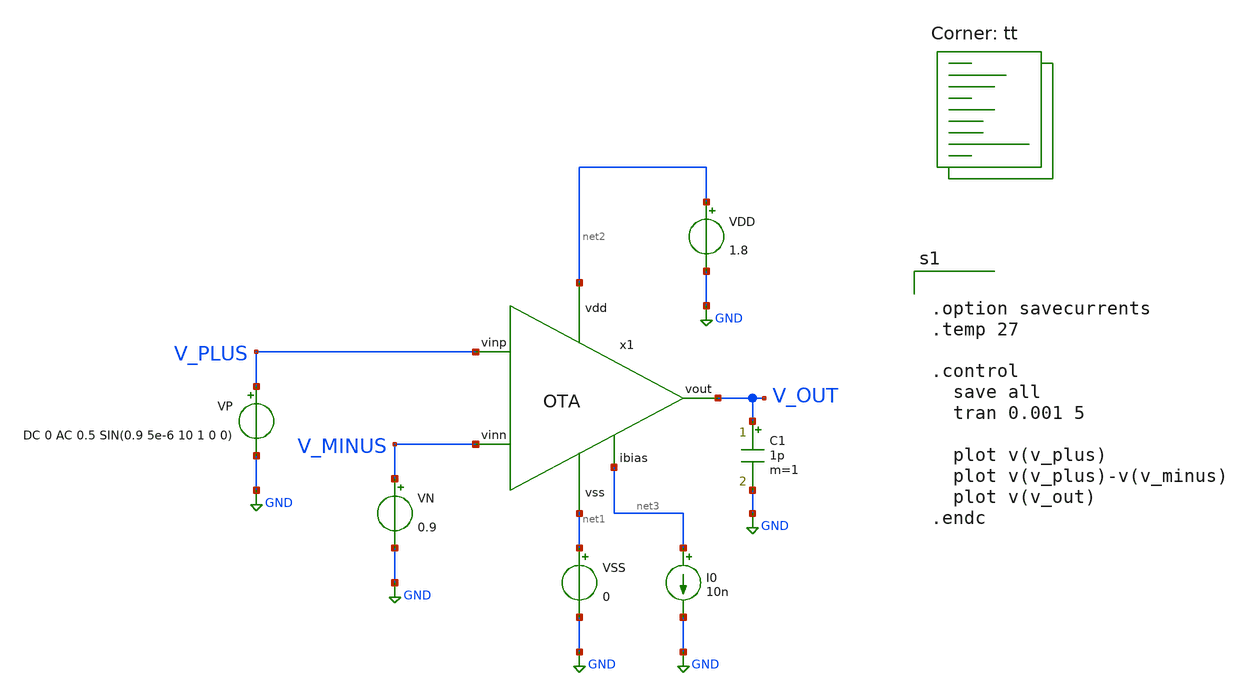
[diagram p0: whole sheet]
** sch_path: Schematic/OTA_Trans_tb.sch
**.subckt OTA_Trans_tb
x1 net2 V_OUT net3 V_MINUS V_PLUS net1 OTA
VDD net2 GND 1.8
VP V_PLUS GND DC 0 AC 0.5 SIN(0.9 5e-6 10 1 0 0)
VN V_MINUS GND 0.9
VSS net1 GND 0
I0 net3 GND 10n
C1 V_OUT GND 1p m=1
**** begin user architecture code


.option savecurrents
.temp 27

.control
  save all
  tran 0.001 5

  plot v(v_plus)
  plot v(v_plus)-v(v_minus)
  plot v(v_out)
.endc



.lib $::SKYWATER_MODELS/sky130.lib.spice tt
**** end user architecture code
**.ends

* expanding   symbol:  /foss/designs/Neuromorphics/Analog_to_Spike/Schematic/OTA.sym # of pins=6
** sym_path: Schematic/OTA.sym
** sch_path: Schematic/OTA.sch
.subckt OTA vdd vout ibias vinn vinp vss
*.ipin vdd
*.ipin vinp
*.ipin vinn
*.ipin vss
*.opin vout
*.ipin ibias
XM1 net1 vinp net3 vdd sky130_fd_pr__pfet_01v8 L=2 W=10 nf=1 ad='int((1 + 1)/2) * 10 / 1 * 0.29' as='int((1 + 2)/2) * 10 / 1 * 0.29'
+ pd='2*int((1 + 1)/2) * (10 / 1 + 0.29)' ps='2*int((1 + 2)/2) * (10 / 1 + 0.29)' nrd='0.29 / 10 ' nrs='0.29 / 10 '
+ sa=0 sb=0 sd=0 mult=1 m=1
XM3 net1 net1 vss vss sky130_fd_pr__nfet_01v8 L=2 W=2 nf=1 ad='int((1 + 1)/2) * 2 / 1 * 0.29' as='int((1 + 2)/2) * 2 / 1 * 0.29'
+ pd='2*int((1 + 1)/2) * (2 / 1 + 0.29)' ps='2*int((1 + 2)/2) * (2 / 1 + 0.29)' nrd='0.29 / 2 ' nrs='0.29 / 2 '
+ sa=0 sb=0 sd=0 mult=1 m=1
XM4 net2 net2 vss vss sky130_fd_pr__nfet_01v8 L=2 W=2 nf=1 ad='int((1 + 1)/2) * 2 / 1 * 0.29' as='int((1 + 2)/2) * 2 / 1 * 0.29'
+ pd='2*int((1 + 1)/2) * (2 / 1 + 0.29)' ps='2*int((1 + 2)/2) * (2 / 1 + 0.29)' nrd='0.29 / 2 ' nrs='0.29 / 2 '
+ sa=0 sb=0 sd=0 mult=1 m=1
XM2 net2 vinn net3 vdd sky130_fd_pr__pfet_01v8 L=2 W=10 nf=1 ad='int((1 + 1)/2) * 10 / 1 * 0.29' as='int((1 + 2)/2) * 10 / 1 * 0.29'
+ pd='2*int((1 + 1)/2) * (10 / 1 + 0.29)' ps='2*int((1 + 2)/2) * (10 / 1 + 0.29)' nrd='0.29 / 10 ' nrs='0.29 / 10 '
+ sa=0 sb=0 sd=0 mult=1 m=1
XM5 net4 net1 vss vss sky130_fd_pr__nfet_01v8 L=2 W=14 nf=1 ad='int((1 + 1)/2) * 14 / 1 * 0.29' as='int((1 + 2)/2) * 14 / 1 * 0.29'
+ pd='2*int((1 + 1)/2) * (14 / 1 + 0.29)' ps='2*int((1 + 2)/2) * (14 / 1 + 0.29)' nrd='0.29 / 14 ' nrs='0.29 / 14 '
+ sa=0 sb=0 sd=0 mult=1 m=1
XM6 vout net2 vss vss sky130_fd_pr__nfet_01v8 L=2 W=14 nf=1 ad='int((1 + 1)/2) * 14 / 1 * 0.29' as='int((1 + 2)/2) * 14 / 1 * 0.29'
+ pd='2*int((1 + 1)/2) * (14 / 1 + 0.29)' ps='2*int((1 + 2)/2) * (14 / 1 + 0.29)' nrd='0.29 / 14 ' nrs='0.29 / 14 '
+ sa=0 sb=0 sd=0 mult=1 m=1
XM7 net4 net4 vdd vdd sky130_fd_pr__pfet_01v8 L=2 W=2 nf=1 ad='int((1 + 1)/2) * 2 / 1 * 0.29' as='int((1 + 2)/2) * 2 / 1 * 0.29'
+ pd='2*int((1 + 1)/2) * (2 / 1 + 0.29)' ps='2*int((1 + 2)/2) * (2 / 1 + 0.29)' nrd='0.29 / 2 ' nrs='0.29 / 2 '
+ sa=0 sb=0 sd=0 mult=1 m=1
XM8 vout net4 vdd vdd sky130_fd_pr__pfet_01v8 L=2 W=2 nf=1 ad='int((1 + 1)/2) * 2 / 1 * 0.29' as='int((1 + 2)/2) * 2 / 1 * 0.29'
+ pd='2*int((1 + 1)/2) * (2 / 1 + 0.29)' ps='2*int((1 + 2)/2) * (2 / 1 + 0.29)' nrd='0.29 / 2 ' nrs='0.29 / 2 '
+ sa=0 sb=0 sd=0 mult=1 m=1
XM10 net3 ibias vdd vdd sky130_fd_pr__pfet_01v8 L=2 W=10 nf=1 ad='int((1 + 1)/2) * 10 / 1 * 0.29' as='int((1 + 2)/2) * 10 / 1 * 0.29'
+ pd='2*int((1 + 1)/2) * (10 / 1 + 0.29)' ps='2*int((1 + 2)/2) * (10 / 1 + 0.29)' nrd='0.29 / 10 ' nrs='0.29 / 10 '
+ sa=0 sb=0 sd=0 mult=1 m=1
XM9 ibias ibias vdd vdd sky130_fd_pr__pfet_01v8 L=2 W=10 nf=1 ad='int((1 + 1)/2) * 10 / 1 * 0.29' as='int((1 + 2)/2) * 10 / 1 * 0.29'
+ pd='2*int((1 + 1)/2) * (10 / 1 + 0.29)' ps='2*int((1 + 2)/2) * (10 / 1 + 0.29)' nrd='0.29 / 10 ' nrs='0.29 / 10 '
+ sa=0 sb=0 sd=0 mult=1 m=1
.ends

.GLOBAL GND
.end
